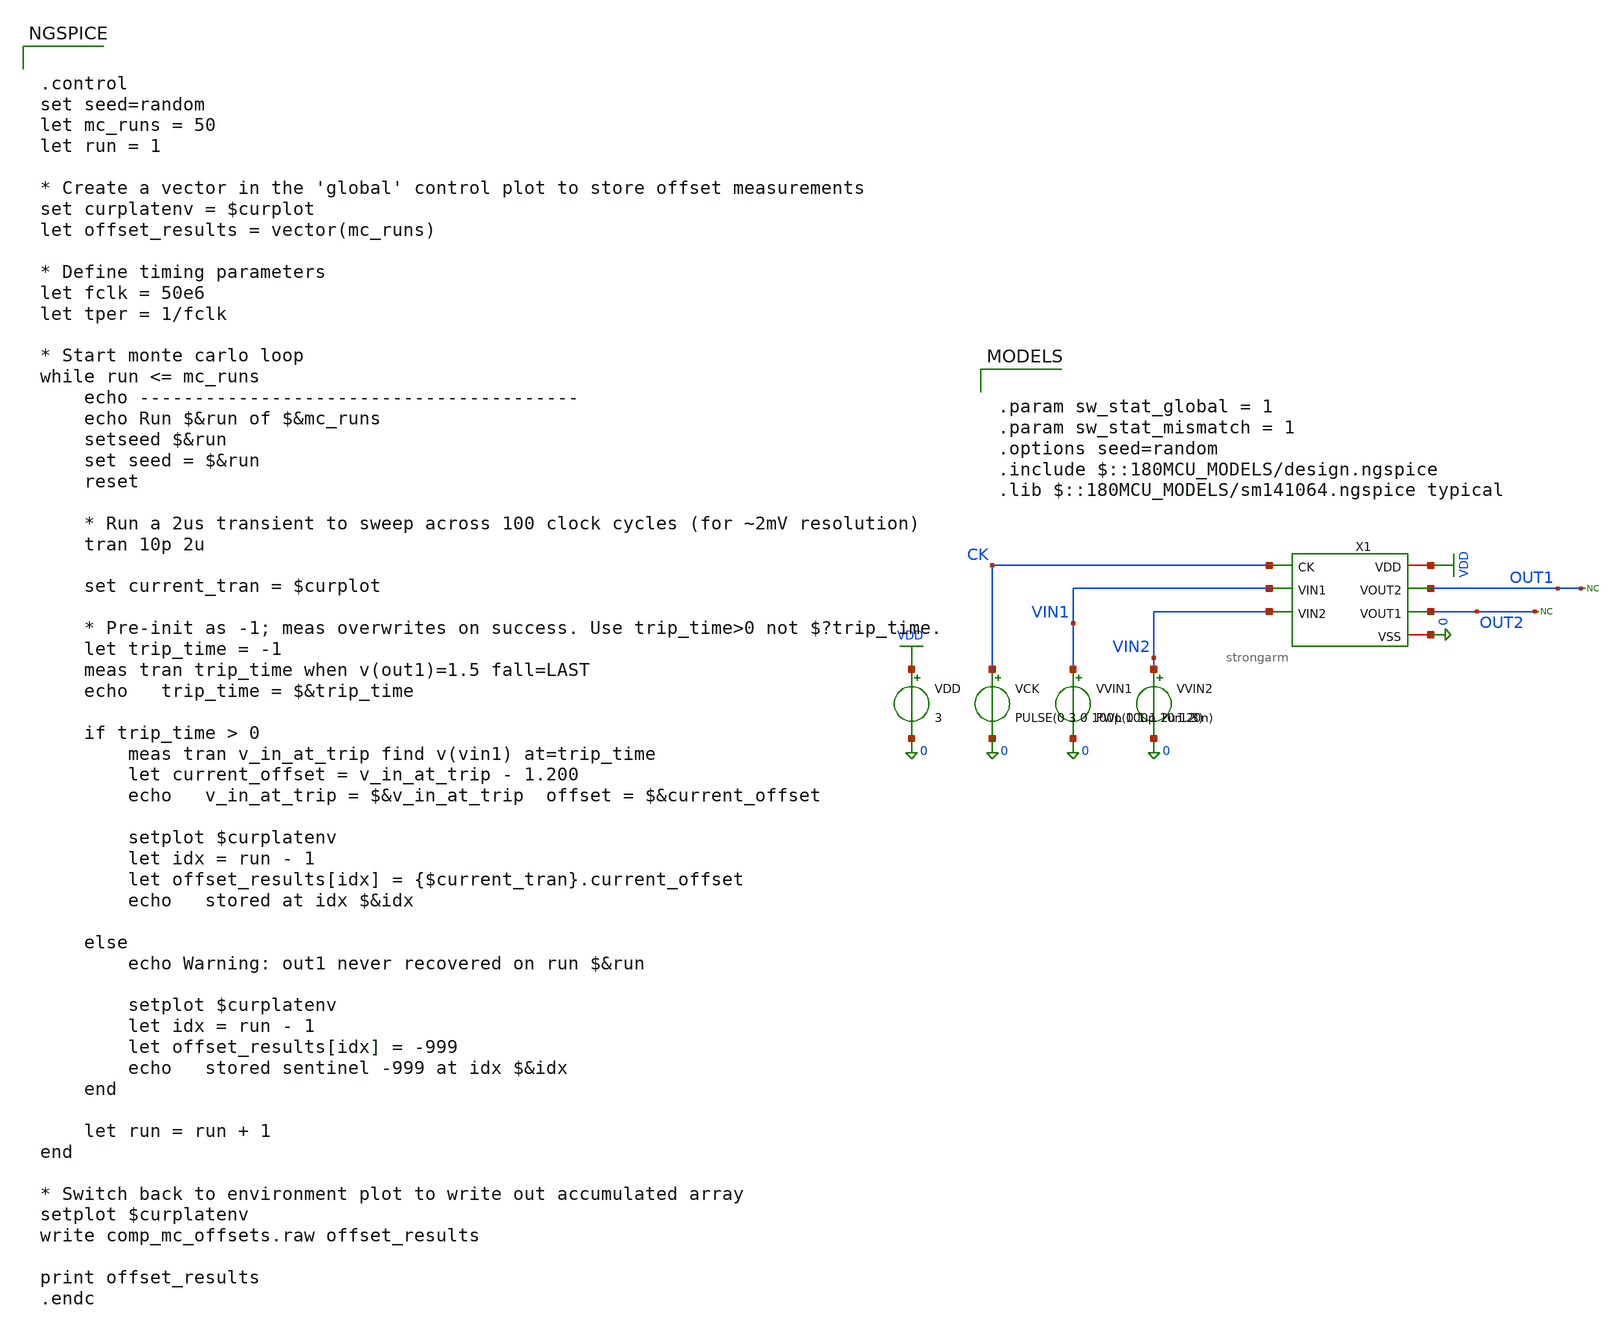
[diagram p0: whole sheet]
** sch_path: comparator/schematic/backup_files/buffer_2.sch
**.subckt buffer_2
X1 VDD CK OUT1 OUT2 VIN1 VIN2 0 strongarm
VVIN2 VIN2 0 1.2
VVIN1 VIN1 0 PWL(0 1.1 2u 1.3)
VDD VDD 0 3
VCK CK 0 PULSE(0 3 0 100p 100p 10n 20n)
* noconn OUT2
* noconn OUT1
**** begin user architecture code

.param sw_stat_global = 1
.param sw_stat_mismatch = 1
.options seed=random
.include $::180MCU_MODELS/design.ngspice
.lib $::180MCU_MODELS/sm141064.ngspice typical



.control
set seed=random
let mc_runs = 50
let run = 1

* Create a vector in the 'global' control plot to store offset measurements
set curplatenv = $curplot
let offset_results = vector(mc_runs)

* Define timing parameters
let fclk = 50e6
let tper = 1/fclk

* Start monte carlo loop
while run <= mc_runs
	echo ----------------------------------------
	echo Run $&run of $&mc_runs
    setseed $&run
    set seed = $&run
	reset

	* Run a 2us transient to sweep across 100 clock cycles (for ~2mV resolution)
	tran 10p 2u

	set current_tran = $curplot

	* Pre-init as -1; meas overwrites on success. Use trip_time>0 not $?trip_time.
	let trip_time = -1
	meas tran trip_time when v(out1)=1.5 fall=LAST
	echo   trip_time = $&trip_time

	if trip_time > 0
		meas tran v_in_at_trip find v(vin1) at=trip_time
		let current_offset = v_in_at_trip - 1.200
		echo   v_in_at_trip = $&v_in_at_trip  offset = $&current_offset

		setplot $curplatenv
		let idx = run - 1
		let offset_results[idx] = {$current_tran}.current_offset
		echo   stored at idx $&idx

	else
		echo Warning: out1 never recovered on run $&run

		setplot $curplatenv
		let idx = run - 1
		let offset_results[idx] = -999
		echo   stored sentinel -999 at idx $&idx
	end

	let run = run + 1
end

* Switch back to environment plot to write out accumulated array
setplot $curplatenv
write comp_mc_offsets.raw offset_results

print offset_results
.endc


**** end user architecture code
**.ends

* expanding   symbol:  comparator/schematic/strongarm.sym # of pins=7
** sym_path: comparator/schematic/strongarm.sym
** sch_path: comparator/schematic/strongarm.sch
.subckt strongarm VDD CK VOUT2 VOUT1 VIN1 VIN2 VSS
*.opin VOUT1
*.opin VOUT2
*.ipin VIN1
*.ipin VIN2
*.ipin CK
*.iopin VDD
*.iopin VSS
XM1 VOUT2 VOUT1 net1 net1 nfet_03v3 L=0.28u W=0.22u nf=1 ad='int((nf+1)/2) * W/nf * 0.18u' as='int((nf+2)/2) * W/nf * 0.18u'
+ pd='2*int((nf+1)/2) * (W/nf + 0.18u)' ps='2*int((nf+2)/2) * (W/nf + 0.18u)' nrd='0.18u / W' nrs='0.18u / W'
+ sa=0 sb=0 sd=0 m=1
XM2 VOUT1 VOUT2 VDD VDD pfet_03v3 L=0.28u W=0.22u nf=1 ad='int((nf+1)/2) * W/nf * 0.18u' as='int((nf+2)/2) * W/nf * 0.18u'
+ pd='2*int((nf+1)/2) * (W/nf + 0.18u)' ps='2*int((nf+2)/2) * (W/nf + 0.18u)' nrd='0.18u / W' nrs='0.18u / W'
+ sa=0 sb=0 sd=0 m=1
XM3 VOUT1 CK VDD VDD pfet_03v3 L=0.28u W=0.22u nf=1 ad='int((nf+1)/2) * W/nf * 0.18u' as='int((nf+2)/2) * W/nf * 0.18u'
+ pd='2*int((nf+1)/2) * (W/nf + 0.18u)' ps='2*int((nf+2)/2) * (W/nf + 0.18u)' nrd='0.18u / W' nrs='0.18u / W'
+ sa=0 sb=0 sd=0 m=1
XM4 net3 CK VDD VDD pfet_03v3 L=0.28u W=0.22u nf=1 ad='int((nf+1)/2) * W/nf * 0.18u' as='int((nf+2)/2) * W/nf * 0.18u'
+ pd='2*int((nf+1)/2) * (W/nf + 0.18u)' ps='2*int((nf+2)/2) * (W/nf + 0.18u)' nrd='0.18u / W' nrs='0.18u / W'
+ sa=0 sb=0 sd=0 m=1
XM5 net1 CK VDD VDD pfet_03v3 L=0.28u W=0.22u nf=1 ad='int((nf+1)/2) * W/nf * 0.18u' as='int((nf+2)/2) * W/nf * 0.18u'
+ pd='2*int((nf+1)/2) * (W/nf + 0.18u)' ps='2*int((nf+2)/2) * (W/nf + 0.18u)' nrd='0.18u / W' nrs='0.18u / W'
+ sa=0 sb=0 sd=0 m=1
XM6 VOUT2 CK VDD VDD pfet_03v3 L=0.28u W=0.22u nf=1 ad='int((nf+1)/2) * W/nf * 0.18u' as='int((nf+2)/2) * W/nf * 0.18u'
+ pd='2*int((nf+1)/2) * (W/nf + 0.18u)' ps='2*int((nf+2)/2) * (W/nf + 0.18u)' nrd='0.18u / W' nrs='0.18u / W'
+ sa=0 sb=0 sd=0 m=1
XM7 VOUT2 VOUT1 VDD VDD pfet_03v3 L=0.28u W=0.22u nf=1 ad='int((nf+1)/2) * W/nf * 0.18u' as='int((nf+2)/2) * W/nf * 0.18u'
+ pd='2*int((nf+1)/2) * (W/nf + 0.18u)' ps='2*int((nf+2)/2) * (W/nf + 0.18u)' nrd='0.18u / W' nrs='0.18u / W'
+ sa=0 sb=0 sd=0 m=1
XM8 net1 VIN2 net2 net2 nfet_03v3 L=0.28u W=0.22u nf=1 ad='int((nf+1)/2) * W/nf * 0.18u' as='int((nf+2)/2) * W/nf * 0.18u'
+ pd='2*int((nf+1)/2) * (W/nf + 0.18u)' ps='2*int((nf+2)/2) * (W/nf + 0.18u)' nrd='0.18u / W' nrs='0.18u / W'
+ sa=0 sb=0 sd=0 m=1
XM9 VOUT1 VOUT2 net3 net3 nfet_03v3 L=0.28u W=0.22u nf=1 ad='int((nf+1)/2) * W/nf * 0.18u' as='int((nf+2)/2) * W/nf * 0.18u'
+ pd='2*int((nf+1)/2) * (W/nf + 0.18u)' ps='2*int((nf+2)/2) * (W/nf + 0.18u)' nrd='0.18u / W' nrs='0.18u / W'
+ sa=0 sb=0 sd=0 m=1
XM10 net3 VIN1 net2 net2 nfet_03v3 L=0.28u W=0.22u nf=1 ad='int((nf+1)/2) * W/nf * 0.18u' as='int((nf+2)/2) * W/nf * 0.18u'
+ pd='2*int((nf+1)/2) * (W/nf + 0.18u)' ps='2*int((nf+2)/2) * (W/nf + 0.18u)' nrd='0.18u / W' nrs='0.18u / W'
+ sa=0 sb=0 sd=0 m=1
XM11 net2 CK VSS net2 nfet_03v3 L=0.28u W=0.22u nf=1 ad='int((nf+1)/2) * W/nf * 0.18u' as='int((nf+2)/2) * W/nf * 0.18u'
+ pd='2*int((nf+1)/2) * (W/nf + 0.18u)' ps='2*int((nf+2)/2) * (W/nf + 0.18u)' nrd='0.18u / W' nrs='0.18u / W'
+ sa=0 sb=0 sd=0 m=1
.ends

.GLOBAL VDD
.end
